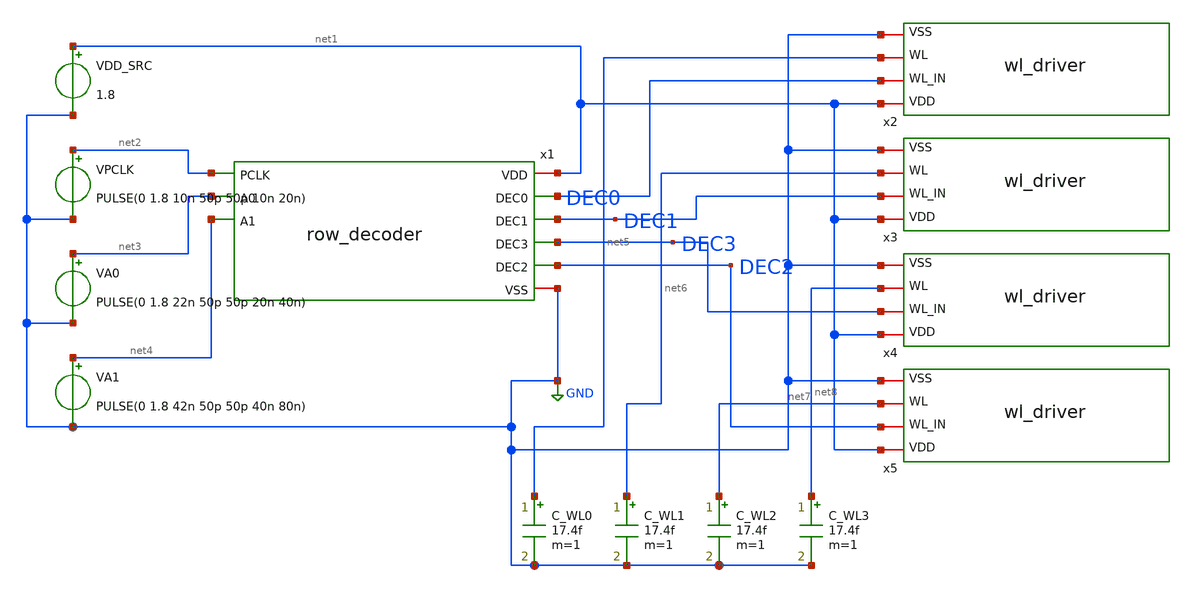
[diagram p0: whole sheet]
** sch_path: sims/row_decoder/results/buffered_b7_candidate/tb_candidate.sch
**.subckt tb_candidate
x1 net1 net2 net3 net4 DEC0 DEC1 DEC3 DEC2 GND row_decoder
VDD_SRC net1 GND 1.8
VPCLK net2 GND PULSE(0 1.8 10n 50p 50p 10n 20n)
VA0 net3 GND PULSE(0 1.8 22n 50p 50p 20n 40n)
VA1 net4 GND PULSE(0 1.8 42n 50p 50p 40n 80n)
x2 net1 DEC0 net5 GND wl_driver
x3 net1 DEC1 net6 GND wl_driver
x4 net1 DEC3 net8 GND wl_driver
x5 net1 DEC2 net7 GND wl_driver
C_WL0 net5 GND 17.4f m=1
C_WL1 net6 GND 17.4f m=1
C_WL2 net7 GND 17.4f m=1
C_WL3 net8 GND 17.4f m=1
**.ends
.GLOBAL GND
.end
